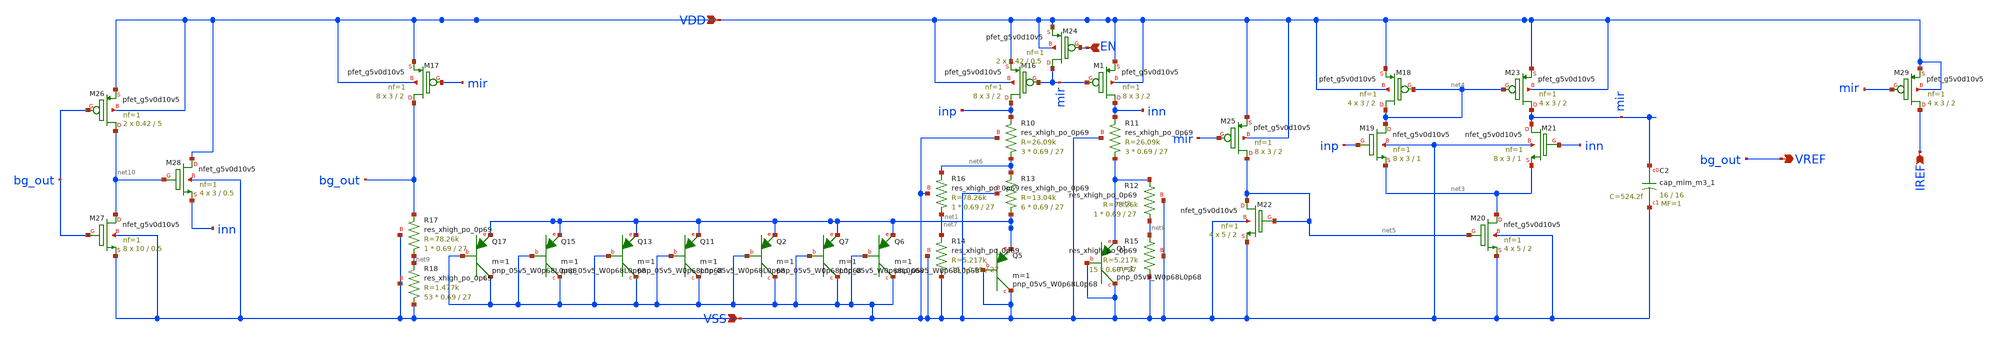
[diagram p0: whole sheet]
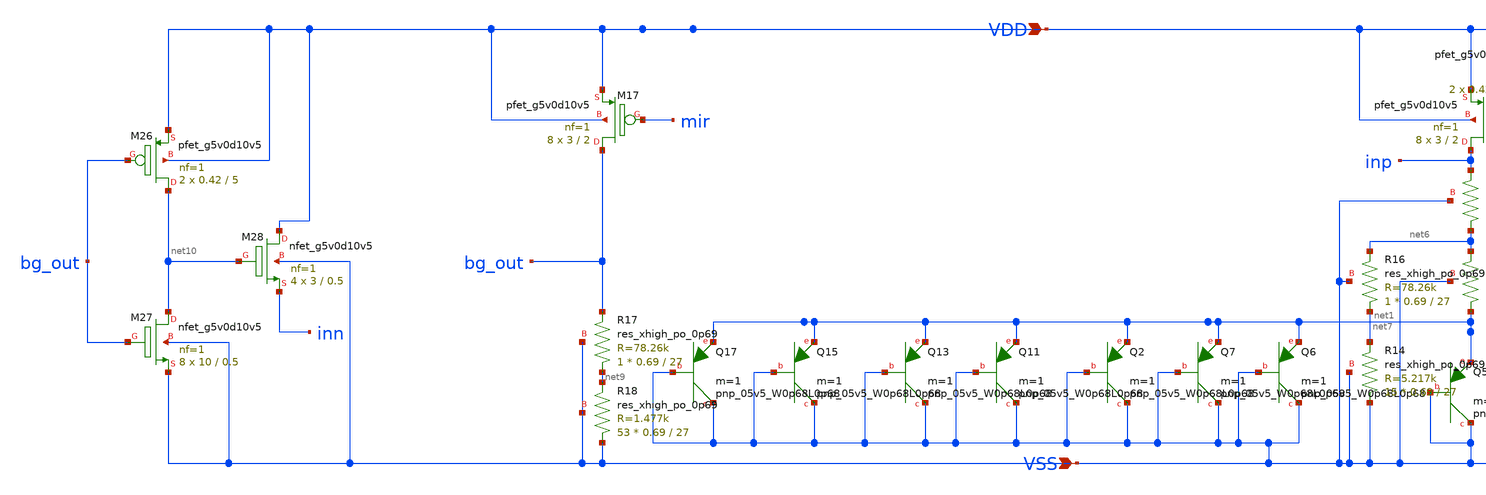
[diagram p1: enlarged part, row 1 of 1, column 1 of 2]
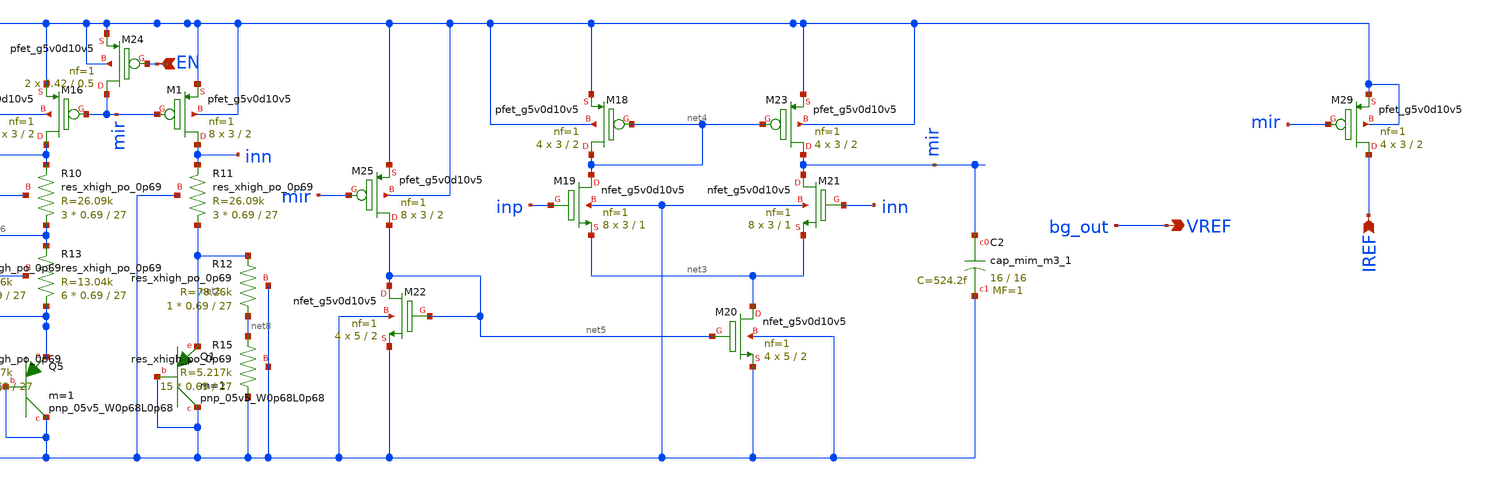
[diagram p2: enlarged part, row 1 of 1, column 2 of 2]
** sch_path: bandgap/bandgap5.sch
**.subckt bandgap5 VDD VSS VREF EN IREF
*.ipin VDD
*.ipin VSS
*.opin VREF
*.ipin EN
*.ipin IREF
XM1 inn mir VDD VDD sky130_fd_pr__pfet_g5v0d10v5 L=2 W=3 nf=1 ad='int((nf+1)/2) * W/nf * 0.29' as='int((nf+2)/2) * W/nf * 0.29'
+ pd='2*int((nf+1)/2) * (W/nf + 0.29)' ps='2*int((nf+2)/2) * (W/nf + 0.29)' nrd='0.29 / W' nrs='0.29 / W'
+ sa=0 sb=0 sd=0 mult=8 m=8
XM16 inp mir VDD VDD sky130_fd_pr__pfet_g5v0d10v5 L=2 W=3 nf=1 ad='int((nf+1)/2) * W/nf * 0.29' as='int((nf+2)/2) * W/nf * 0.29'
+ pd='2*int((nf+1)/2) * (W/nf + 0.29)' ps='2*int((nf+2)/2) * (W/nf + 0.29)' nrd='0.29 / W' nrs='0.29 / W'
+ sa=0 sb=0 sd=0 mult=8 m=8
XM17 bg_out mir VDD VDD sky130_fd_pr__pfet_g5v0d10v5 L=2 W=3 nf=1 ad='int((nf+1)/2) * W/nf * 0.29' as='int((nf+2)/2) * W/nf * 0.29'
+ pd='2*int((nf+1)/2) * (W/nf + 0.29)' ps='2*int((nf+2)/2) * (W/nf + 0.29)' nrd='0.29 / W' nrs='0.29 / W'
+ sa=0 sb=0 sd=0 mult=8 m=8
XQ1 VSS VSS net2 sky130_fd_pr__pnp_05v5_W0p68L0p68 m=1
XQ5 VSS VSS net1 sky130_fd_pr__pnp_05v5_W0p68L0p68 m=1
XQ6 VSS VSS net1 sky130_fd_pr__pnp_05v5_W0p68L0p68 m=1
XQ7 VSS VSS net1 sky130_fd_pr__pnp_05v5_W0p68L0p68 m=1
XQ2 VSS VSS net1 sky130_fd_pr__pnp_05v5_W0p68L0p68 m=1
XQ11 VSS VSS net1 sky130_fd_pr__pnp_05v5_W0p68L0p68 m=1
XQ13 VSS VSS net1 sky130_fd_pr__pnp_05v5_W0p68L0p68 m=1
XQ15 VSS VSS net1 sky130_fd_pr__pnp_05v5_W0p68L0p68 m=1
XQ17 VSS VSS net1 sky130_fd_pr__pnp_05v5_W0p68L0p68 m=1
XM18 net4 net4 VDD VDD sky130_fd_pr__pfet_g5v0d10v5 L=2 W=3 nf=1 ad='int((nf+1)/2) * W/nf * 0.29' as='int((nf+2)/2) * W/nf * 0.29'
+ pd='2*int((nf+1)/2) * (W/nf + 0.29)' ps='2*int((nf+2)/2) * (W/nf + 0.29)' nrd='0.29 / W' nrs='0.29 / W'
+ sa=0 sb=0 sd=0 mult=4 m=4
XM19 net4 inp net3 VSS sky130_fd_pr__nfet_g5v0d10v5 L=1 W=3 nf=1 ad='int((nf+1)/2) * W/nf * 0.29' as='int((nf+2)/2) * W/nf * 0.29'
+ pd='2*int((nf+1)/2) * (W/nf + 0.29)' ps='2*int((nf+2)/2) * (W/nf + 0.29)' nrd='0.29 / W' nrs='0.29 / W'
+ sa=0 sb=0 sd=0 mult=8 m=8
XM21 mir inn net3 VSS sky130_fd_pr__nfet_g5v0d10v5 L=1 W=3 nf=1 ad='int((nf+1)/2) * W/nf * 0.29' as='int((nf+2)/2) * W/nf * 0.29'
+ pd='2*int((nf+1)/2) * (W/nf + 0.29)' ps='2*int((nf+2)/2) * (W/nf + 0.29)' nrd='0.29 / W' nrs='0.29 / W'
+ sa=0 sb=0 sd=0 mult=8 m=8
XM23 mir net4 VDD VDD sky130_fd_pr__pfet_g5v0d10v5 L=2 W=3 nf=1 ad='int((nf+1)/2) * W/nf * 0.29' as='int((nf+2)/2) * W/nf * 0.29'
+ pd='2*int((nf+1)/2) * (W/nf + 0.29)' ps='2*int((nf+2)/2) * (W/nf + 0.29)' nrd='0.29 / W' nrs='0.29 / W'
+ sa=0 sb=0 sd=0 mult=4 m=4
XM20 net3 net5 VSS VSS sky130_fd_pr__nfet_g5v0d10v5 L=2 W=5 nf=1 ad='int((nf+1)/2) * W/nf * 0.29' as='int((nf+2)/2) * W/nf * 0.29'
+ pd='2*int((nf+1)/2) * (W/nf + 0.29)' ps='2*int((nf+2)/2) * (W/nf + 0.29)' nrd='0.29 / W' nrs='0.29 / W'
+ sa=0 sb=0 sd=0 mult=4 m=4
XM25 net5 mir VDD VDD sky130_fd_pr__pfet_g5v0d10v5 L=2 W=3 nf=1 ad='int((nf+1)/2) * W/nf * 0.29' as='int((nf+2)/2) * W/nf * 0.29'
+ pd='2*int((nf+1)/2) * (W/nf + 0.29)' ps='2*int((nf+2)/2) * (W/nf + 0.29)' nrd='0.29 / W' nrs='0.29 / W'
+ sa=0 sb=0 sd=0 mult=8 m=8
XM22 net5 net5 VSS VSS sky130_fd_pr__nfet_g5v0d10v5 L=2 W=5 nf=1 ad='int((nf+1)/2) * W/nf * 0.29' as='int((nf+2)/2) * W/nf * 0.29'
+ pd='2*int((nf+1)/2) * (W/nf + 0.29)' ps='2*int((nf+2)/2) * (W/nf + 0.29)' nrd='0.29 / W' nrs='0.29 / W'
+ sa=0 sb=0 sd=0 mult=4 m=4
XC2 mir VSS sky130_fd_pr__cap_mim_m3_1 W=16 L=16 MF=1 m=1
XR10 net6 inp VSS sky130_fd_pr__res_xhigh_po_0p69 L=27 mult=3 m=3
XR11 net2 inn VSS sky130_fd_pr__res_xhigh_po_0p69 L=27 mult=3 m=3
XR12 net8 net2 VSS sky130_fd_pr__res_xhigh_po_0p69 L=27 mult=1 m=1
XR13 net1 net6 VSS sky130_fd_pr__res_xhigh_po_0p69 L=27 mult=6 m=6
XR14 VSS net7 VSS sky130_fd_pr__res_xhigh_po_0p69 L=27 mult=15 m=15
XR15 VSS net8 VSS sky130_fd_pr__res_xhigh_po_0p69 L=27 mult=15 m=15
XR16 net7 net6 VSS sky130_fd_pr__res_xhigh_po_0p69 L=27 mult=1 m=1
XR17 net9 bg_out VSS sky130_fd_pr__res_xhigh_po_0p69 L=27 mult=1 m=1
XR18 VSS net9 VSS sky130_fd_pr__res_xhigh_po_0p69 L=27 mult=53 m=53
XM24 mir EN VDD VDD sky130_fd_pr__pfet_g5v0d10v5 L=0.5 W=0.42 nf=1 ad='int((nf+1)/2) * W/nf * 0.29' as='int((nf+2)/2) * W/nf * 0.29'
+ pd='2*int((nf+1)/2) * (W/nf + 0.29)' ps='2*int((nf+2)/2) * (W/nf + 0.29)' nrd='0.29 / W' nrs='0.29 / W'
+ sa=0 sb=0 sd=0 mult=2 m=2
XM26 net10 bg_out VDD VDD sky130_fd_pr__pfet_g5v0d10v5 L=5 W=0.42 nf=1 ad='int((nf+1)/2) * W/nf * 0.29'
+ as='int((nf+2)/2) * W/nf * 0.29' pd='2*int((nf+1)/2) * (W/nf + 0.29)' ps='2*int((nf+2)/2) * (W/nf + 0.29)'
+ nrd='0.29 / W' nrs='0.29 / W' sa=0 sb=0 sd=0 mult=2 m=2
XM27 net10 bg_out VSS VSS sky130_fd_pr__nfet_g5v0d10v5 L=0.5 W=10 nf=1 ad='int((nf+1)/2) * W/nf * 0.29'
+ as='int((nf+2)/2) * W/nf * 0.29' pd='2*int((nf+1)/2) * (W/nf + 0.29)' ps='2*int((nf+2)/2) * (W/nf + 0.29)'
+ nrd='0.29 / W' nrs='0.29 / W' sa=0 sb=0 sd=0 mult=8 m=8
XM28 VDD net10 inn VSS sky130_fd_pr__nfet_g5v0d10v5 L=0.5 W=3 nf=1 ad='int((nf+1)/2) * W/nf * 0.29' as='int((nf+2)/2) * W/nf * 0.29'
+ pd='2*int((nf+1)/2) * (W/nf + 0.29)' ps='2*int((nf+2)/2) * (W/nf + 0.29)' nrd='0.29 / W' nrs='0.29 / W'
+ sa=0 sb=0 sd=0 mult=4 m=4
XM29 IREF mir VDD VDD sky130_fd_pr__pfet_g5v0d10v5 L=2 W=3 nf=1 ad='int((nf+1)/2) * W/nf * 0.29' as='int((nf+2)/2) * W/nf * 0.29'
+ pd='2*int((nf+1)/2) * (W/nf + 0.29)' ps='2*int((nf+2)/2) * (W/nf + 0.29)' nrd='0.29 / W' nrs='0.29 / W'
+ sa=0 sb=0 sd=0 mult=4 m=4
**.ends
.end
